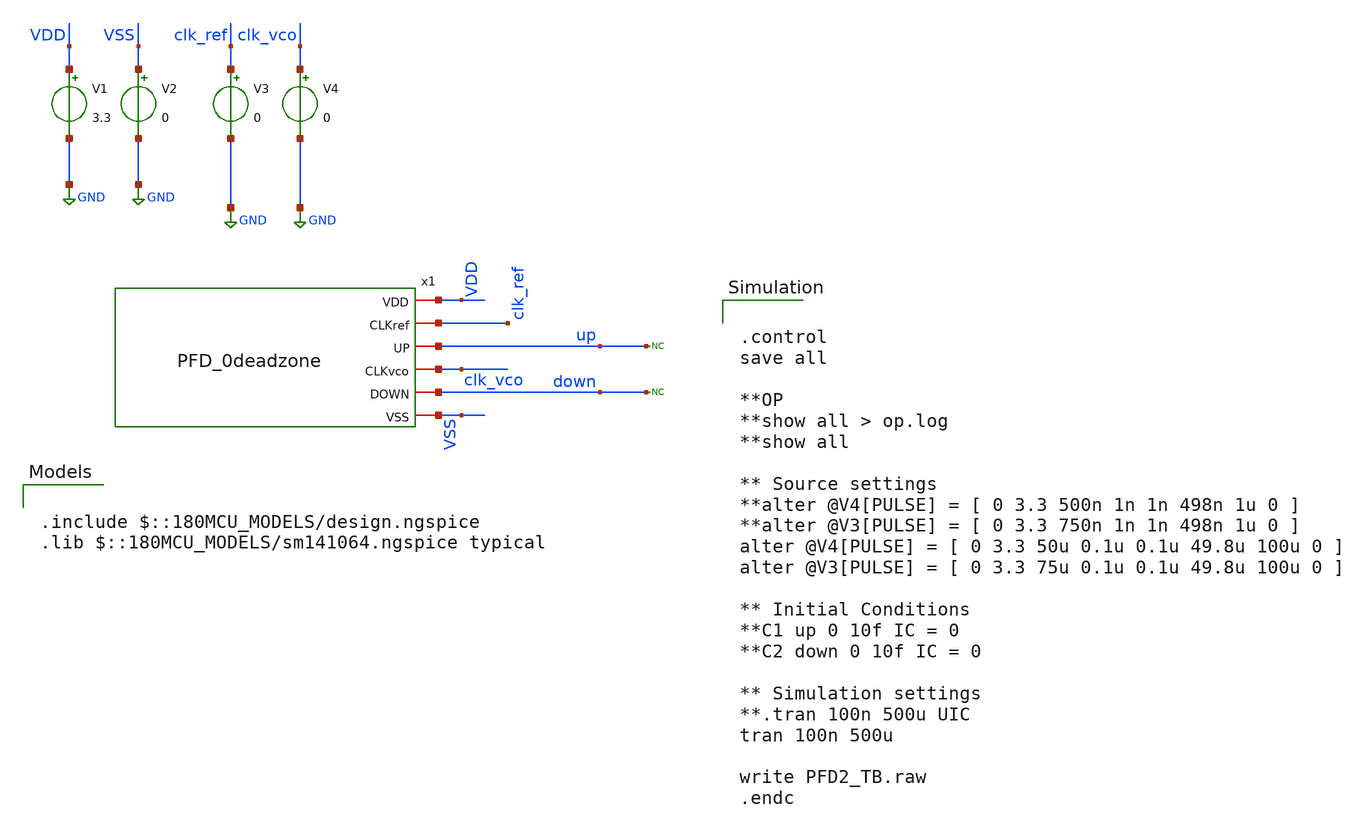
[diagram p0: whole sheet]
** sch_path: designs/libs/xp_core_analog/PFD_new/PFD2_TB.sch
**.subckt PFD2_TB
x1 VDD clk_ref up clk_vco down VSS PFD_0deadzone
V1 VDD GND 3.3
V2 VSS GND 0
* noconn up
* noconn down
V3 clk_ref GND 0
V4 clk_vco GND 0
**** begin user architecture code

.include $::180MCU_MODELS/design.ngspice
.lib $::180MCU_MODELS/sm141064.ngspice typical



.control
save all

**OP
**show all > op.log
**show all

** Source settings
**alter @V4[PULSE] = [ 0 3.3 500n 1n 1n 498n 1u 0 ]
**alter @V3[PULSE] = [ 0 3.3 750n 1n 1n 498n 1u 0 ]
alter @V4[PULSE] = [ 0 3.3 50u 0.1u 0.1u 49.8u 100u 0 ]
alter @V3[PULSE] = [ 0 3.3 75u 0.1u 0.1u 49.8u 100u 0 ]

** Initial Conditions
**C1 up 0 10f IC = 0
**C2 down 0 10f IC = 0

** Simulation settings
**.tran 100n 500u UIC
tran 100n 500u

write PFD2_TB.raw
.endc


**** end user architecture code
**.ends
.GLOBAL GND
.end
